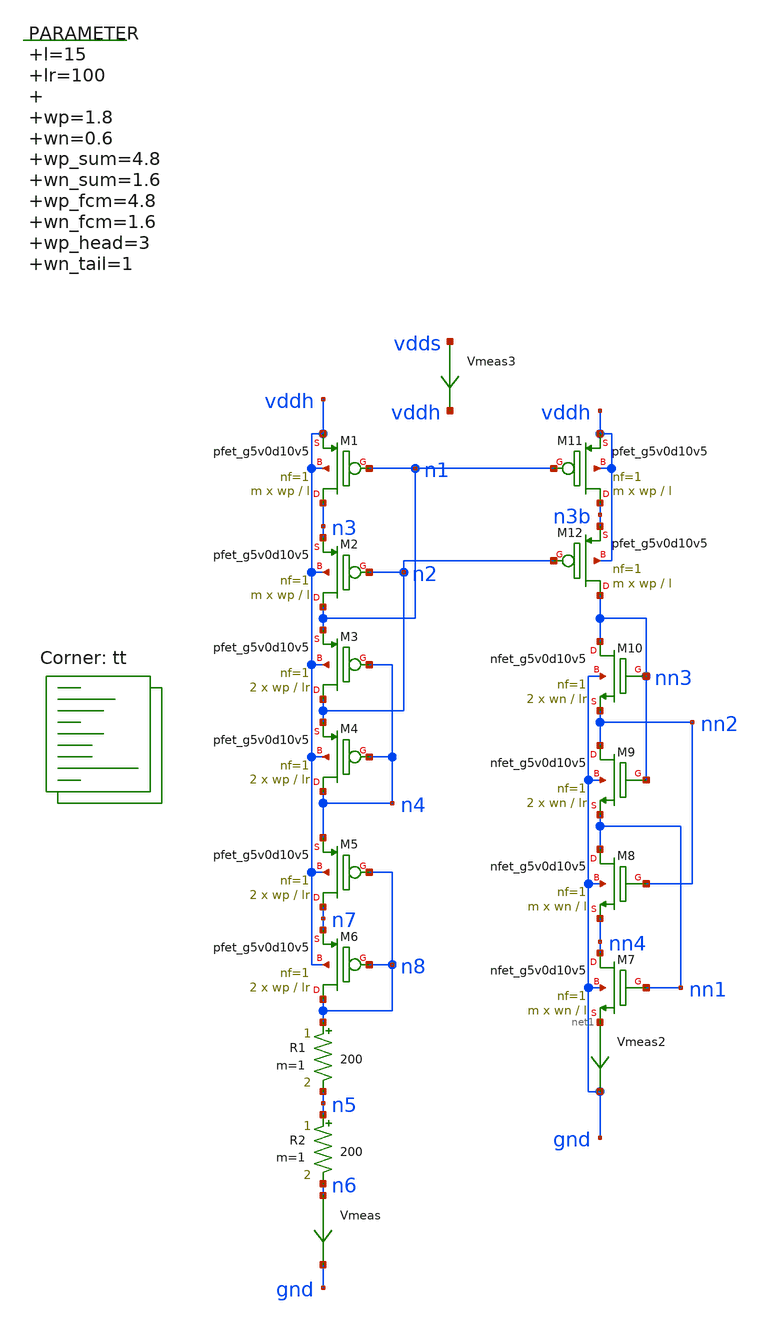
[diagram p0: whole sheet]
** sch_path: xschem/current_mirror_characterization-tb.sch
**.subckt current_mirror_characterization-tb
XM1 n3 n1 vddh vddh sky130_fd_pr__pfet_g5v0d10v5 L=l W=wp nf=1 ad='int((nf+1)/2) * W/nf * 0.29' as='int((nf+2)/2) * W/nf * 0.29'
+ pd='2*int((nf+1)/2) * (W/nf + 0.29)' ps='2*int((nf+2)/2) * (W/nf + 0.29)' nrd='0.29 / W' nrs='0.29 / W'
+ sa=0 sb=0 sd=0 mult=m m=m
.param l=15 lr=100 wp=1.8 wn=0.6 wp_sum=4.8 wn_sum=1.6 wp_fcm=4.8 wn_fcm=1.6 wp_head=3 wn_tail=1
+ wp_bsum=4.8 wn_bsum=1.6 m=10 m1=5 m_sum=2 m_refsum=5 m_fcm=2 mdiff0=2
Vmeas n6 gnd 0
.save i(vmeas)
R1 n8 n5 200 m=1
R2 n5 n6 200 m=1
XM2 n1 n2 n3 vddh sky130_fd_pr__pfet_g5v0d10v5 L=l W=wp nf=1 ad='int((nf+1)/2) * W/nf * 0.29' as='int((nf+2)/2) * W/nf * 0.29'
+ pd='2*int((nf+1)/2) * (W/nf + 0.29)' ps='2*int((nf+2)/2) * (W/nf + 0.29)' nrd='0.29 / W' nrs='0.29 / W'
+ sa=0 sb=0 sd=0 mult=m m=m
XM3 n2 n4 n1 vddh sky130_fd_pr__pfet_g5v0d10v5 L=lr W=wp nf=1 ad='int((nf+1)/2) * W/nf * 0.29' as='int((nf+2)/2) * W/nf * 0.29'
+ pd='2*int((nf+1)/2) * (W/nf + 0.29)' ps='2*int((nf+2)/2) * (W/nf + 0.29)' nrd='0.29 / W' nrs='0.29 / W'
+ sa=0 sb=0 sd=0 mult=2 m=2
XM4 n4 n4 n2 vddh sky130_fd_pr__pfet_g5v0d10v5 L=lr W=wp nf=1 ad='int((nf+1)/2) * W/nf * 0.29' as='int((nf+2)/2) * W/nf * 0.29'
+ pd='2*int((nf+1)/2) * (W/nf + 0.29)' ps='2*int((nf+2)/2) * (W/nf + 0.29)' nrd='0.29 / W' nrs='0.29 / W'
+ sa=0 sb=0 sd=0 mult=2 m=2
XM5 n7 n8 n4 vddh sky130_fd_pr__pfet_g5v0d10v5 L=lr W=wp nf=1 ad='int((nf+1)/2) * W/nf * 0.29' as='int((nf+2)/2) * W/nf * 0.29'
+ pd='2*int((nf+1)/2) * (W/nf + 0.29)' ps='2*int((nf+2)/2) * (W/nf + 0.29)' nrd='0.29 / W' nrs='0.29 / W'
+ sa=0 sb=0 sd=0 mult=2 m=2
XM6 n8 n8 n7 vddh sky130_fd_pr__pfet_g5v0d10v5 L=lr W=wp nf=1 ad='int((nf+1)/2) * W/nf * 0.29' as='int((nf+2)/2) * W/nf * 0.29'
+ pd='2*int((nf+1)/2) * (W/nf + 0.29)' ps='2*int((nf+2)/2) * (W/nf + 0.29)' nrd='0.29 / W' nrs='0.29 / W'
+ sa=0 sb=0 sd=0 mult=2 m=2
XM7 nn4 nn1 net1 gnd sky130_fd_pr__nfet_g5v0d10v5 L=l W=wn nf=1 ad='int((nf+1)/2) * W/nf * 0.29' as='int((nf+2)/2) * W/nf * 0.29'
+ pd='2*int((nf+1)/2) * (W/nf + 0.29)' ps='2*int((nf+2)/2) * (W/nf + 0.29)' nrd='0.29 / W' nrs='0.29 / W'
+ sa=0 sb=0 sd=0 mult=m m=m
XM8 nn1 nn2 nn4 gnd sky130_fd_pr__nfet_g5v0d10v5 L=l W=wn nf=1 ad='int((nf+1)/2) * W/nf * 0.29' as='int((nf+2)/2) * W/nf * 0.29'
+ pd='2*int((nf+1)/2) * (W/nf + 0.29)' ps='2*int((nf+2)/2) * (W/nf + 0.29)' nrd='0.29 / W' nrs='0.29 / W'
+ sa=0 sb=0 sd=0 mult=m m=m
XM9 nn2 nn3 nn1 gnd sky130_fd_pr__nfet_g5v0d10v5 L=lr W=wn nf=1 ad='int((nf+1)/2) * W/nf * 0.29' as='int((nf+2)/2) * W/nf * 0.29'
+ pd='2*int((nf+1)/2) * (W/nf + 0.29)' ps='2*int((nf+2)/2) * (W/nf + 0.29)' nrd='0.29 / W' nrs='0.29 / W'
+ sa=0 sb=0 sd=0 mult=2 m=2
XM10 nn3 nn3 nn2 gnd sky130_fd_pr__nfet_g5v0d10v5 L=lr W=wn nf=1 ad='int((nf+1)/2) * W/nf * 0.29' as='int((nf+2)/2) * W/nf * 0.29'
+ pd='2*int((nf+1)/2) * (W/nf + 0.29)' ps='2*int((nf+2)/2) * (W/nf + 0.29)' nrd='0.29 / W' nrs='0.29 / W'
+ sa=0 sb=0 sd=0 mult=2 m=2
Vmeas2 net1 gnd 0
.save i(vmeas2)
XM11 n3b n1 vddh vddh sky130_fd_pr__pfet_g5v0d10v5 L=l W=wp nf=1 ad='int((nf+1)/2) * W/nf * 0.29' as='int((nf+2)/2) * W/nf * 0.29'
+ pd='2*int((nf+1)/2) * (W/nf + 0.29)' ps='2*int((nf+2)/2) * (W/nf + 0.29)' nrd='0.29 / W' nrs='0.29 / W'
+ sa=0 sb=0 sd=0 mult=m m=m
XM12 nn3 n2 n3b vddh sky130_fd_pr__pfet_g5v0d10v5 L=l W=wp nf=1 ad='int((nf+1)/2) * W/nf * 0.29' as='int((nf+2)/2) * W/nf * 0.29'
+ pd='2*int((nf+1)/2) * (W/nf + 0.29)' ps='2*int((nf+2)/2) * (W/nf + 0.29)' nrd='0.29 / W' nrs='0.29 / W'
+ sa=0 sb=0 sd=0 mult=m m=m
Vmeas3 vdds vddh 0
.save i(vmeas3)
**** begin user architecture code
.lib $::SKYWATER_MODELS/sky130.lib.spice tt



  .option wnflag=1
  .option safecurrents
  ********************Static Current Sources***************************
  .param iref=10u
  *Iref n4 gnd 100n
  ********************Static Voltage Sources***************************
  Vddh vdds gnd dc 5.5
  ********************Simulation Commands*****************************
  .control
     reset
     save all
     *tran 0.1p 300p
     dc R2 1meg 2meg 1k
     write current_mirror-tb.raw
     set appendwrite
*    quit 0
  .endc



**** end user architecture code
**.ends
.end
